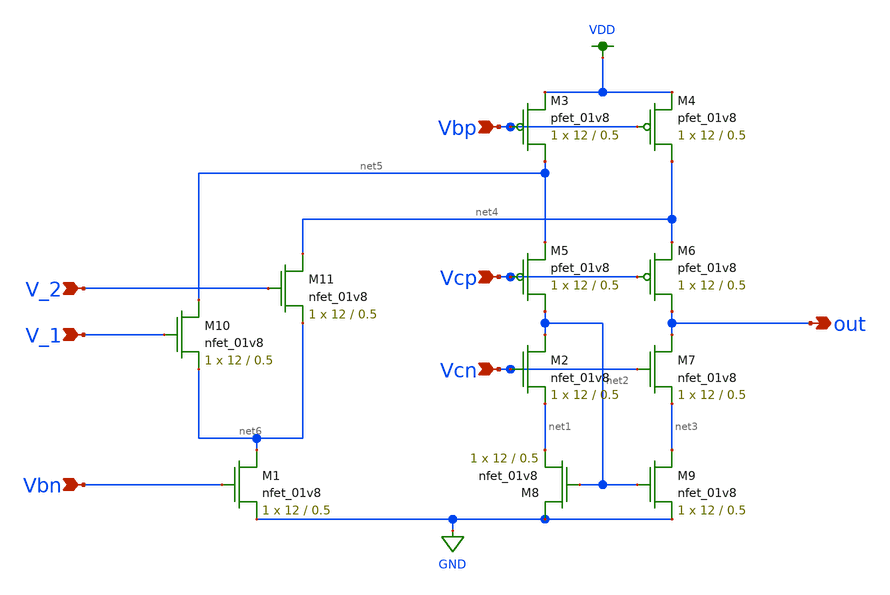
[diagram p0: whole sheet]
** sch_path: miniproject3/f_cascode_diff_amp.sch
**.subckt f_cascode_diff_amp V_1 V_2 Vcp Vcn out Vbp Vbn
*.ipin V_1
*.ipin V_2
*.ipin Vcp
*.ipin Vcn
*.opin out
*.ipin Vbp
*.ipin Vbn
XM11 net4 V_2 net6 GND sky130_fd_pr__nfet_01v8 L=0.5 W=12 nf=1 ad='int((nf+1)/2) * W/nf * 0.29' as='int((nf+2)/2) * W/nf * 0.29'
+ pd='2*int((nf+1)/2) * (W/nf + 0.29)' ps='2*int((nf+2)/2) * (W/nf + 0.29)' nrd='0.29 / W' nrs='0.29 / W'
+ sa=0 sb=0 sd=0 mult=1 m=1
XM10 net5 V_1 net6 GND sky130_fd_pr__nfet_01v8 L=0.5 W=12 nf=1 ad='int((nf+1)/2) * W/nf * 0.29' as='int((nf+2)/2) * W/nf * 0.29'
+ pd='2*int((nf+1)/2) * (W/nf + 0.29)' ps='2*int((nf+2)/2) * (W/nf + 0.29)' nrd='0.29 / W' nrs='0.29 / W'
+ sa=0 sb=0 sd=0 mult=1 m=1
XM1 net6 Vbn GND GND sky130_fd_pr__nfet_01v8 L=0.5 W=12 nf=1 ad='int((nf+1)/2) * W/nf * 0.29' as='int((nf+2)/2) * W/nf * 0.29'
+ pd='2*int((nf+1)/2) * (W/nf + 0.29)' ps='2*int((nf+2)/2) * (W/nf + 0.29)' nrd='0.29 / W' nrs='0.29 / W'
+ sa=0 sb=0 sd=0 mult=1 m=1
XM8 GND net2 net1 GND sky130_fd_pr__nfet_01v8 L=0.5 W=12 nf=1 ad='int((nf+1)/2) * W/nf * 0.29' as='int((nf+2)/2) * W/nf * 0.29'
+ pd='2*int((nf+1)/2) * (W/nf + 0.29)' ps='2*int((nf+2)/2) * (W/nf + 0.29)' nrd='0.29 / W' nrs='0.29 / W'
+ sa=0 sb=0 sd=0 mult=1 m=1
XM9 net3 net2 GND GND sky130_fd_pr__nfet_01v8 L=0.5 W=12 nf=1 ad='int((nf+1)/2) * W/nf * 0.29' as='int((nf+2)/2) * W/nf * 0.29'
+ pd='2*int((nf+1)/2) * (W/nf + 0.29)' ps='2*int((nf+2)/2) * (W/nf + 0.29)' nrd='0.29 / W' nrs='0.29 / W'
+ sa=0 sb=0 sd=0 mult=1 m=1
XM7 out Vcn net3 GND sky130_fd_pr__nfet_01v8 L=0.5 W=12 nf=1 ad='int((nf+1)/2) * W/nf * 0.29' as='int((nf+2)/2) * W/nf * 0.29'
+ pd='2*int((nf+1)/2) * (W/nf + 0.29)' ps='2*int((nf+2)/2) * (W/nf + 0.29)' nrd='0.29 / W' nrs='0.29 / W'
+ sa=0 sb=0 sd=0 mult=1 m=1
XM2 net2 Vcn net1 GND sky130_fd_pr__nfet_01v8 L=0.5 W=12 nf=1 ad='int((nf+1)/2) * W/nf * 0.29' as='int((nf+2)/2) * W/nf * 0.29'
+ pd='2*int((nf+1)/2) * (W/nf + 0.29)' ps='2*int((nf+2)/2) * (W/nf + 0.29)' nrd='0.29 / W' nrs='0.29 / W'
+ sa=0 sb=0 sd=0 mult=1 m=1
XM5 net2 Vcp net5 VDD sky130_fd_pr__pfet_01v8 L=0.5 W=12 nf=1 ad='int((nf+1)/2) * W/nf * 0.29' as='int((nf+2)/2) * W/nf * 0.29'
+ pd='2*int((nf+1)/2) * (W/nf + 0.29)' ps='2*int((nf+2)/2) * (W/nf + 0.29)' nrd='0.29 / W' nrs='0.29 / W'
+ sa=0 sb=0 sd=0 mult=1 m=1
XM6 out Vcp net4 VDD sky130_fd_pr__pfet_01v8 L=0.5 W=12 nf=1 ad='int((nf+1)/2) * W/nf * 0.29' as='int((nf+2)/2) * W/nf * 0.29'
+ pd='2*int((nf+1)/2) * (W/nf + 0.29)' ps='2*int((nf+2)/2) * (W/nf + 0.29)' nrd='0.29 / W' nrs='0.29 / W'
+ sa=0 sb=0 sd=0 mult=1 m=1
XM4 net4 Vbp VDD VDD sky130_fd_pr__pfet_01v8 L=0.5 W=12 nf=1 ad='int((nf+1)/2) * W/nf * 0.29' as='int((nf+2)/2) * W/nf * 0.29'
+ pd='2*int((nf+1)/2) * (W/nf + 0.29)' ps='2*int((nf+2)/2) * (W/nf + 0.29)' nrd='0.29 / W' nrs='0.29 / W'
+ sa=0 sb=0 sd=0 mult=1 m=1
XM3 net5 Vbp VDD VDD sky130_fd_pr__pfet_01v8 L=0.5 W=12 nf=1 ad='int((nf+1)/2) * W/nf * 0.29' as='int((nf+2)/2) * W/nf * 0.29'
+ pd='2*int((nf+1)/2) * (W/nf + 0.29)' ps='2*int((nf+2)/2) * (W/nf + 0.29)' nrd='0.29 / W' nrs='0.29 / W'
+ sa=0 sb=0 sd=0 mult=1 m=1
**.ends
.GLOBAL VDD
.GLOBAL GND
.end
